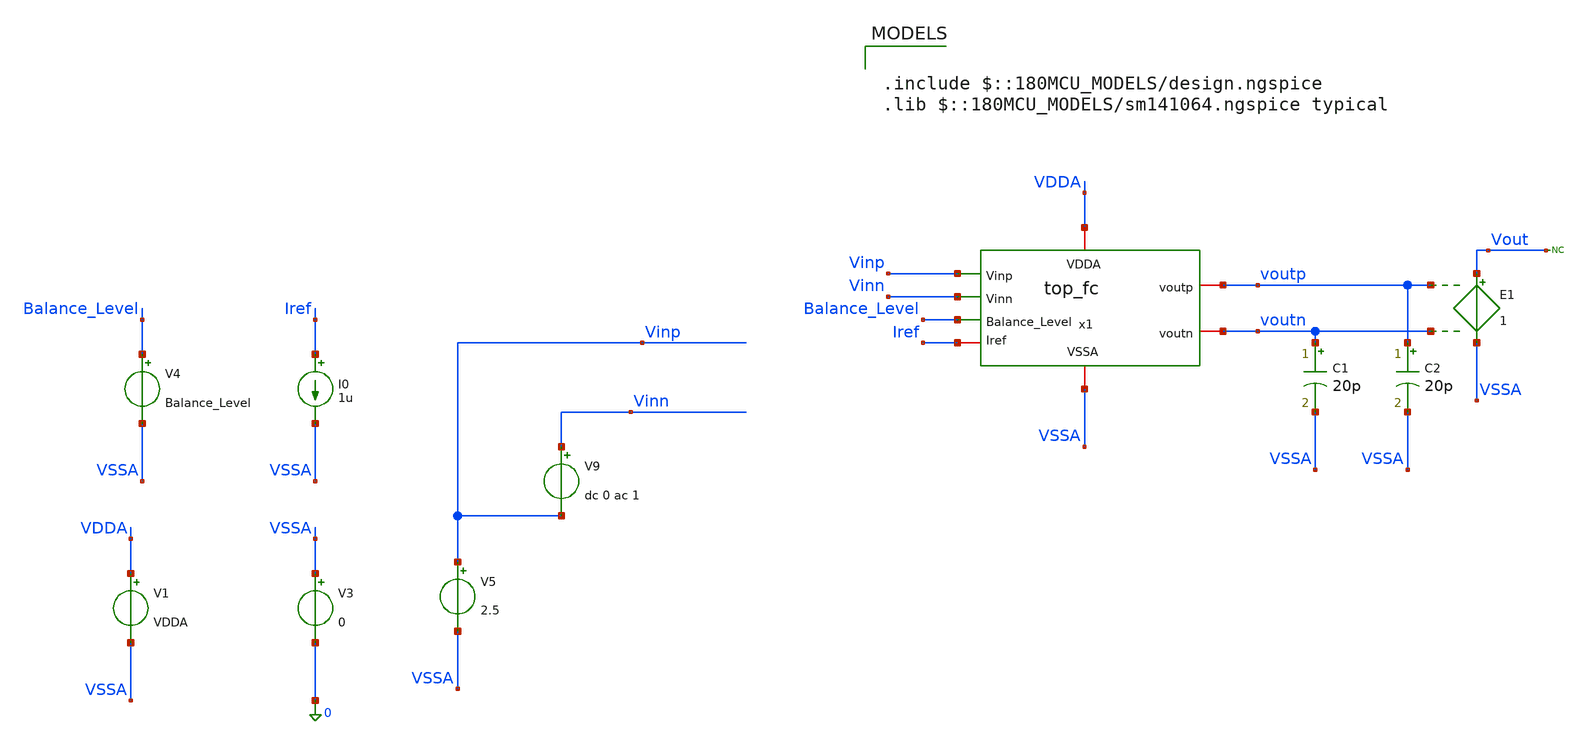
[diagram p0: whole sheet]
** sch_path: Folded_cascode/testbenches/top_fc_ac_tb.sch
**.subckt top_fc_ac_tb
x1 Balance_Level Vinp voutp VDDA voutn Vinn Iref VSSA top_fc
C1 voutn VSSA 20p m=1
C2 voutp VSSA 20p m=1
V1 VDDA VSSA VDDA
V3 VSSA 0 0
V4 Balance_Level VSSA Balance_Level
I0 Iref VSSA 1u
V5 Vinp VSSA 2.5
V9 Vinn Vinp dc 0 ac 1
E1 Vout VSSA voutp voutn 1
* noconn Vout
**** begin user architecture code

.include $::180MCU_MODELS/design.ngspice
.lib $::180MCU_MODELS/sm141064.ngspice typical



.temp 27
.param VDDA = 5
.param Balance_Level = 1.5

.control
option sparse
set filetype=ascii
set wr_singlescale
set wr_vecnames
save all
save @m.x1.x1.xm1.m0[id]
save @m.x1.x1.xm1.m0[gm]
save @m.x1.x1.xm1.m0[vgs]
save @m.x1.x1.xm1.m0[vds]
save @m.x1.x1.xm1.m0[vth]
save @m.x1.x1.xm1.m0[gds]
save @m.x1.x1.xm1.m0[vdsat]

save @m.x1.x1.xm2.m0[id]
save @m.x1.x1.xm2.m0[gm]
save @m.x1.x1.xm2.m0[vgs]
save @m.x1.x1.xm2.m0[vds]
save @m.x1.x1.xm2.m0[vth]
save @m.x1.x1.xm2.m0[gds]
save @m.x1.x1.xm2.m0[vdsat]

save @m.x1.x1.xm9.m0[id]
save @m.x1.x1.xm9.m0[gm]
save @m.x1.x1.xm9.m0[vgs]
save @m.x1.x1.xm9.m0[vds]
save @m.x1.x1.xm9.m0[vth]
save @m.x1.x1.xm9.m0[gds]
save @m.x1.x1.xm9.m0[vdsat]

save @m.x1.x1.xm8.m0[id]
save @m.x1.x1.xm8.m0[gm]
save @m.x1.x1.xm8.m0[vgs]
save @m.x1.x1.xm8.m0[vds]
save @m.x1.x1.xm8.m0[vth]
save @m.x1.x1.xm8.m0[gds]
save @m.x1.x1.xm8.m0[vdsat]

save @m.x1.x1.xm6.m0[id]
save @m.x1.x1.xm6.m0[gm]
save @m.x1.x1.xm6.m0[vgs]
save @m.x1.x1.xm6.m0[vds]
save @m.x1.x1.xm6.m0[vth]
save @m.x1.x1.xm6.m0[gds]
save @m.x1.x1.xm6.m0[vdsat]

save @m.x1.x1.xm5.m0[id]
save @m.x1.x1.xm5.m0[gm]
save @m.x1.x1.xm5.m0[vgs]
save @m.x1.x1.xm5.m0[vds]
save @m.x1.x1.xm5.m0[vth]
save @m.x1.x1.xm5.m0[gds]
save @m.x1.x1.xm5.m0[vdsat]

save @m.x1.x2.xm1.m0[id]
save @m.x1.x2.xm1.m0[gm]
save @m.x1.x2.xm1.m0[vgs]
save @m.x1.x2.xm1.m0[vds]
save @m.x1.x2.xm1.m0[vth]
save @m.x1.x2.xm1.m0[gds]

save @m.x1.x2.xm2.m0[id]
save @m.x1.x2.xm2.m0[gm]
save @m.x1.x2.xm2.m0[vgs]
save @m.x1.x2.xm2.m0[vds]
save @m.x1.x2.xm2.m0[vth]
save @m.x1.x2.xm2.m0[gds]

save @m.x1.x2.xm3.m0[id]
save @m.x1.x2.xm3.m0[gm]
save @m.x1.x2.xm3.m0[vgs]
save @m.x1.x2.xm3.m0[vds]
save @m.x1.x2.xm3.m0[vth]
save @m.x1.x2.xm3.m0[gds]

save @m.x1.x2.xm4.m0[id]
save @m.x1.x2.xm4.m0[gm]
save @m.x1.x2.xm4.m0[vgs]
save @m.x1.x2.xm4.m0[vds]
save @m.x1.x2.xm4.m0[vth]
save @m.x1.x2.xm4.m0[gds]

save @m.x1.x2.xm5.m0[id]
save @m.x1.x2.xm5.m0[gm]
save @m.x1.x2.xm5.m0[vgs]
save @m.x1.x2.xm5.m0[vds]
save @m.x1.x2.xm5.m0[vth]
save @m.x1.x2.xm5.m0[gds]

save @m.x1.x2.xm6.m0[id]
save @m.x1.x2.xm6.m0[gm]
save @m.x1.x2.xm6.m0[vgs]
save @m.x1.x2.xm6.m0[vds]
save @m.x1.x2.xm6.m0[vth]
save @m.x1.x2.xm6.m0[gds]

save @m.x1.x2.xm7.m0[id]
save @m.x1.x2.xm7.m0[gm]
save @m.x1.x2.xm7.m0[vgs]
save @m.x1.x2.xm7.m0[vds]
save @m.x1.x2.xm7.m0[vth]
save @m.x1.x2.xm7.m0[gds]

save @m.x1.x2.xm8.m0[id]
save @m.x1.x2.xm8.m0[gm]
save @m.x1.x2.xm8.m0[vgs]
save @m.x1.x2.xm8.m0[vds]
save @m.x1.x2.xm8.m0[vth]
save @m.x1.x2.xm8.m0[gds]

save @m.x1.x2.xm9.m0[id]
save @m.x1.x2.xm9.m0[gm]
save @m.x1.x2.xm9.m0[vgs]
save @m.x1.x2.xm9.m0[vds]
save @m.x1.x2.xm9.m0[vth]
save @m.x1.x2.xm9.m0[gds]

save @m.x1.x3.xm1.m0[id]
save @m.x1.x3.xm1.m0[gm]
save @m.x1.x3.xm1.m0[vgs]
save @m.x1.x3.xm1.m0[vds]
save @m.x1.x3.xm1.m0[vth]
save @m.x1.x3.xm1.m0[gds]

save @m.x1.x3.xm2.m0[id]
save @m.x1.x3.xm2.m0[gm]
save @m.x1.x3.xm2.m0[vgs]
save @m.x1.x3.xm2.m0[vds]
save @m.x1.x3.xm2.m0[vth]
save @m.x1.x3.xm2.m0[gds]

save @m.x1.x3.xm3.m0[id]
save @m.x1.x3.xm3.m0[gm]
save @m.x1.x3.xm3.m0[vgs]
save @m.x1.x3.xm3.m0[vds]
save @m.x1.x3.xm3.m0[vth]
save @m.x1.x3.xm3.m0[gds]

save @m.x1.x3.xm4.m0[id]
save @m.x1.x3.xm4.m0[gm]
save @m.x1.x3.xm4.m0[vgs]
save @m.x1.x3.xm4.m0[vds]
save @m.x1.x3.xm4.m0[vth]
save @m.x1.x3.xm4.m0[gds]

save @m.x1.x3.xm5.m0[id]
save @m.x1.x3.xm5.m0[gm]
save @m.x1.x3.xm5.m0[vgs]
save @m.x1.x3.xm5.m0[vds]
save @m.x1.x3.xm5.m0[vth]
save @m.x1.x3.xm5.m0[gds]

save @m.x1.x3.xm6.m0[id]
save @m.x1.x3.xm6.m0[gm]
save @m.x1.x3.xm6.m0[vgs]
save @m.x1.x3.xm6.m0[vds]
save @m.x1.x3.xm6.m0[vth]
save @m.x1.x3.xm6.m0[gds]

save @m.x1.x3.xm7.m0[id]
save @m.x1.x3.xm7.m0[gm]
save @m.x1.x3.xm7.m0[vgs]
save @m.x1.x3.xm7.m0[vds]
save @m.x1.x3.xm7.m0[vth]
save @m.x1.x3.xm7.m0[gds]

save @m.x1.x3.xm8.m0[id]
save @m.x1.x3.xm8.m0[gm]
save @m.x1.x3.xm8.m0[vgs]
save @m.x1.x3.xm8.m0[vds]
save @m.x1.x3.xm8.m0[vth]
save @m.x1.x3.xm8.m0[gds]

save @m.x1.x3.xm9.m0[id]
save @m.x1.x3.xm9.m0[gm]
save @m.x1.x3.xm9.m0[vgs]
save @m.x1.x3.xm9.m0[vds]
save @m.x1.x3.xm9.m0[vth]
save @m.x1.x3.xm9.m0[gds]

save @m.x1.x3.xm10.m0[id]
save @m.x1.x3.xm10.m0[gm]
save @m.x1.x3.xm10.m0[vgs]
save @m.x1.x3.xm10.m0[vds]
save @m.x1.x3.xm10.m0[vth]
save @m.x1.x3.xm10.m0[gds]

save @m.x1.x3.xm11.m0[id]
save @m.x1.x3.xm11.m0[gm]
save @m.x1.x3.xm11.m0[vgs]
save @m.x1.x3.xm11.m0[vds]
save @m.x1.x3.xm11.m0[vth]
save @m.x1.x3.xm11.m0[gds]

save @m.x1.x3.xm12.m0[id]
save @m.x1.x3.xm12.m0[gm]
save @m.x1.x3.xm12.m0[vgs]
save @m.x1.x3.xm12.m0[vds]
save @m.x1.x3.xm12.m0[vth]
save @m.x1.x3.xm12.m0[gds]

save @m.x1.x3.xm13.m0[id]
save @m.x1.x3.xm13.m0[gm]
save @m.x1.x3.xm13.m0[vgs]
save @m.x1.x3.xm13.m0[vds]
save @m.x1.x3.xm13.m0[vth]
save @m.x1.x3.xm13.m0[gds]

save @m.x1.x3.xm14.m0[id]
save @m.x1.x3.xm14.m0[gm]
save @m.x1.x3.xm14.m0[vgs]
save @m.x1.x3.xm14.m0[vds]
save @m.x1.x3.xm14.m0[vth]
save @m.x1.x3.xm14.m0[gds]

save @m.x1.x3.xm15.m0[id]
save @m.x1.x3.xm15.m0[gm]
save @m.x1.x3.xm15.m0[vgs]
save @m.x1.x3.xm15.m0[vds]
save @m.x1.x3.xm15.m0[vth]
save @m.x1.x3.xm15.m0[gds]

save @m.x1.x3.xm16.m0[id]
save @m.x1.x3.xm16.m0[gm]
save @m.x1.x3.xm16.m0[vgs]
save @m.x1.x3.xm16.m0[vds]
save @m.x1.x3.xm16.m0[vth]
save @m.x1.x3.xm16.m0[gds]

save @m.x1.x3.xm17.m0[id]
save @m.x1.x3.xm17.m0[gm]
save @m.x1.x3.xm17.m0[vgs]
save @m.x1.x3.xm17.m0[vds]
save @m.x1.x3.xm17.m0[vth]
save @m.x1.x3.xm17.m0[gds]

save @m.x1.x3.xm18.m0[id]
save @m.x1.x3.xm18.m0[gm]
save @m.x1.x3.xm18.m0[vgs]
save @m.x1.x3.xm18.m0[vds]
save @m.x1.x3.xm18.m0[vth]
save @m.x1.x3.xm18.m0[gds]

save @m.x1.x3.xm21.m0[id]
save @m.x1.x3.xm21.m0[gm]
save @m.x1.x3.xm21.m0[vgs]
save @m.x1.x3.xm21.m0[vds]
save @m.x1.x3.xm21.m0[vth]
save @m.x1.x3.xm21.m0[gds]

save @m.x1.x3.xm22.m0[id]
save @m.x1.x3.xm22.m0[gm]
save @m.x1.x3.xm22.m0[vgs]
save @m.x1.x3.xm22.m0[vds]
save @m.x1.x3.xm22.m0[vth]
save @m.x1.x3.xm22.m0[gds]

op
write top_fc_op_tb.raw all

set appendwrite
ac dec 100 1 1G

* Differential input/output
let vid = v(vinp) - v(vinn)
let vod = v(voutp) - v(voutn)

* Differential gain
let ad = vod / vid

* Magnitude and phase
let gain_db = db(ad)
let phase_deg = (180/pi)*ph(ad)

* Plots
plot gain_db
plot phase_deg

* DC / low-frequency gain
meas ac gain_dc FIND gain_db AT=1

* Unity-gain frequency
meas ac fu WHEN gain_db=0 CROSS=1

* Phase at unity gain
meas ac phase_fu FIND phase_deg AT=fu

* Phase margin
let pm = 180 + phase_fu

print gain_dc
print fu
print phase_fu
print pm

write top_fc_ac_tb.raw

.endc


**** end user architecture code
**.ends
.end
